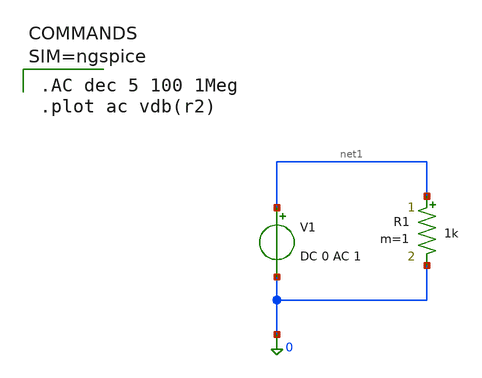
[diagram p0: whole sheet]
** sch_path: tests/bridge/ac_test.sch
**.subckt ac_test
R1 net1 0 1k m=1
V1 net1 0 DC 0 AC 1
**** begin user architecture code


.AC dec 5 100 1Meg
.plot ac vdb(r2)



**** end user architecture code
**.ends
.end
